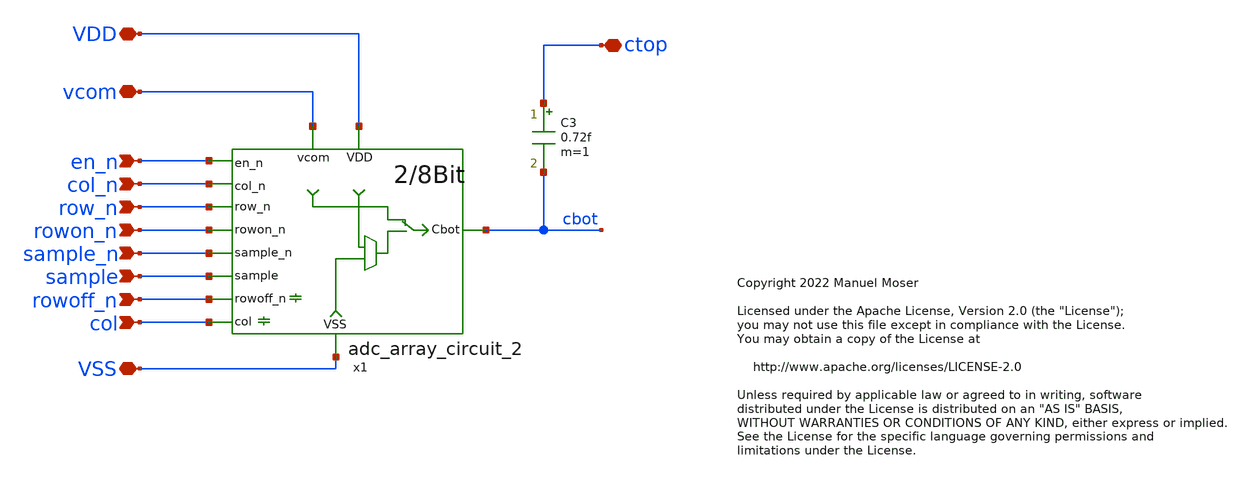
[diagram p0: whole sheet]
** sch_path: xschem/adc_array_wafflecap_8_2.sch
* Copyright 2022 Manuel Moser
* Licensed under the Apache License, Version 2.0 (the "License");
**.subckt adc_array_wafflecap_8_2 vcom VDD ctop VSS en_n row_n col_n rowon_n sample_n sample col
*+ rowoff_n
*.iopin vcom
*.iopin VDD
*.iopin ctop
*.iopin VSS
*.ipin en_n
*.ipin row_n
*.ipin col_n
*.ipin rowon_n
*.ipin sample_n
*.ipin sample
*.ipin col
*.ipin rowoff_n
C3 ctop cbot 0.72f m=1
x1 VDD col_n cbot row_n rowon_n sample_n vcom sample VSS en_n rowoff_n col adc_array_circuit_2
**.ends

* expanding   symbol:  adc_array_circuit_2.sym # of pins=12
** sym_path: xschem/adc_array_circuit_2.sym
** sch_path: xschem/adc_array_circuit_2.sch
.subckt adc_array_circuit_2 VDD col_n Cbot row_n rowon_n sample_n vcom sample VSS en_n rowoff_n col
*.ipin sample_n
*.ipin sample
*.iopin vcom
*.ipin rowoff_n
*.ipin row_n
*.ipin rowon_n
*.iopin VDD
*.iopin VSS
*.iopin Cbot
*.ipin en_n
*.ipin col
*.ipin col_n
XM1 vcom sample Cbot VSS sky130_fd_pr__nfet_01v8 L=0.15 W=0.42 nf=1 ad='int((nf+1)/2) * W/nf * 0.29'
+ as='int((nf+2)/2) * W/nf * 0.29' pd='2*int((nf+1)/2) * (W/nf + 0.29)' ps='2*int((nf+2)/2) * (W/nf + 0.29)'
+ nrd='0.29 / W' nrs='0.29 / W' sa=0 sb=0 sd=0 mult=1 m=1
XM3 vcom sample_n Cbot VDD sky130_fd_pr__pfet_01v8 L=0.15 W=0.8 nf=1 ad='int((nf+1)/2) * W/nf * 0.29'
+ as='int((nf+2)/2) * W/nf * 0.29' pd='2*int((nf+1)/2) * (W/nf + 0.29)' ps='2*int((nf+2)/2) * (W/nf + 0.29)'
+ nrd='0.29 / W' nrs='0.29 / W' sa=0 sb=0 sd=0 mult=1 m=1
XM2 vdrv sample_n Cbot VSS sky130_fd_pr__nfet_01v8 L=0.15 W=0.42 nf=1 ad='int((nf+1)/2) * W/nf * 0.29'
+ as='int((nf+2)/2) * W/nf * 0.29' pd='2*int((nf+1)/2) * (W/nf + 0.29)' ps='2*int((nf+2)/2) * (W/nf + 0.29)'
+ nrd='0.29 / W' nrs='0.29 / W' sa=0 sb=0 sd=0 mult=1 m=1
XM4 vdrv sample Cbot VDD sky130_fd_pr__pfet_01v8 L=0.15 W=0.8 nf=1 ad='int((nf+1)/2) * W/nf * 0.29' as='int((nf+2)/2) * W/nf * 0.29'
+ pd='2*int((nf+1)/2) * (W/nf + 0.29)' ps='2*int((nf+2)/2) * (W/nf + 0.29)' nrd='0.29 / W' nrs='0.29 / W'
+ sa=0 sb=0 sd=0 mult=1 m=1
XM5 vint1 en_n vdrv VDD sky130_fd_pr__pfet_01v8 L=0.15 W=0.8 nf=1 ad='int((nf+1)/2) * W/nf * 0.29' as='int((nf+2)/2) * W/nf * 0.29'
+ pd='2*int((nf+1)/2) * (W/nf + 0.29)' ps='2*int((nf+2)/2) * (W/nf + 0.29)' nrd='0.29 / W' nrs='0.29 / W'
+ sa=0 sb=0 sd=0 mult=1 m=1
XM6 VDD en_n vint1 VDD sky130_fd_pr__pfet_01v8 L=0.15 W=0.8 nf=1 ad='int((nf+1)/2) * W/nf * 0.29' as='int((nf+2)/2) * W/nf * 0.29'
+ pd='2*int((nf+1)/2) * (W/nf + 0.29)' ps='2*int((nf+2)/2) * (W/nf + 0.29)' nrd='0.29 / W' nrs='0.29 / W'
+ sa=0 sb=0 sd=0 mult=1 m=1
XM7 VDD en_n vdrv VDD sky130_fd_pr__pfet_01v8 L=0.15 W=0.8 nf=1 ad='int((nf+1)/2) * W/nf * 0.29' as='int((nf+2)/2) * W/nf * 0.29'
+ pd='2*int((nf+1)/2) * (W/nf + 0.29)' ps='2*int((nf+2)/2) * (W/nf + 0.29)' nrd='0.29 / W' nrs='0.29 / W'
+ sa=0 sb=0 sd=0 mult=1 m=1
XM8 vint2 en_n vdrv VSS sky130_fd_pr__nfet_01v8 L=0.15 W=0.42 nf=1 ad='int((nf+1)/2) * W/nf * 0.29' as='int((nf+2)/2) * W/nf * 0.29'
+ pd='2*int((nf+1)/2) * (W/nf + 0.29)' ps='2*int((nf+2)/2) * (W/nf + 0.29)' nrd='0.29 / W' nrs='0.29 / W'
+ sa=0 sb=0 sd=0 mult=1 m=1
XM9 VSS en_n vint2 VSS sky130_fd_pr__nfet_01v8 L=0.15 W=0.42 nf=1 ad='int((nf+1)/2) * W/nf * 0.29' as='int((nf+2)/2) * W/nf * 0.29'
+ pd='2*int((nf+1)/2) * (W/nf + 0.29)' ps='2*int((nf+2)/2) * (W/nf + 0.29)' nrd='0.29 / W' nrs='0.29 / W'
+ sa=0 sb=0 sd=0 mult=1 m=1
XM10 VSS en_n vint2 VSS sky130_fd_pr__nfet_01v8 L=0.15 W=0.42 nf=1 ad='int((nf+1)/2) * W/nf * 0.29' as='int((nf+2)/2) * W/nf * 0.29'
+ pd='2*int((nf+1)/2) * (W/nf + 0.29)' ps='2*int((nf+2)/2) * (W/nf + 0.29)' nrd='0.29 / W' nrs='0.29 / W'
+ sa=0 sb=0 sd=0 mult=1 m=1
* noconn rowoff_n
* noconn row_n
* noconn rowon_n
* noconn col
* noconn col_n
.ends

.end
